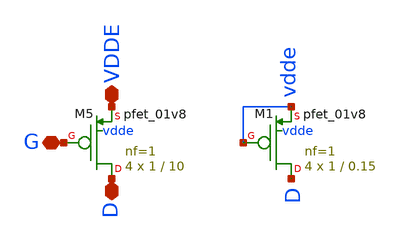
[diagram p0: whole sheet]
** sch_path: magic/pmos_iptat.sch
**.subckt pmos_iptat D G VDDE
*.iopin D
*.iopin G
*.iopin VDDE
XM5 D G VDDE vdde sky130_fd_pr__pfet_01v8 L=10 W=1 nf=1 ad='int((nf+1)/2) * W/nf * 0.29' as='int((nf+2)/2) * W/nf * 0.29'
+ pd='2*int((nf+1)/2) * (W/nf + 0.29)' ps='2*int((nf+2)/2) * (W/nf + 0.29)' nrd='0.29 / W' nrs='0.29 / W'
+ sa=0 sb=0 sd=0 mult=4 m=4
XM1 D vdde vdde vdde sky130_fd_pr__pfet_01v8 L=0.15 W=1 nf=1 ad='int((nf+1)/2) * W/nf * 0.29' as='int((nf+2)/2) * W/nf * 0.29'
+ pd='2*int((nf+1)/2) * (W/nf + 0.29)' ps='2*int((nf+2)/2) * (W/nf + 0.29)' nrd='0.29 / W' nrs='0.29 / W'
+ sa=0 sb=0 sd=0 mult=4 m=4
**.ends
.end
